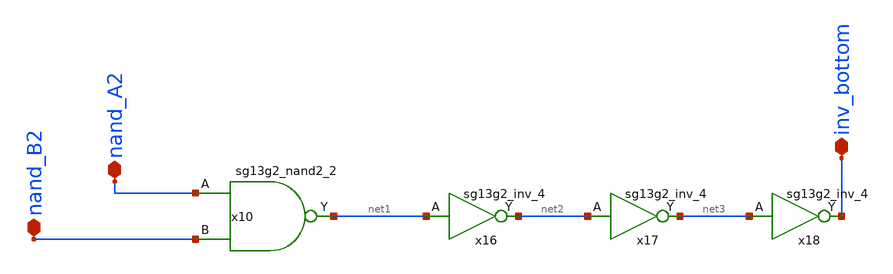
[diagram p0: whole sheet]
** sch_path: 5_Design/4_Layout/Team 5/xschem/clock_5_split4.sch
* IHP-GmbH/IHP-Open-PDK/ihp-sg13g2/libs.tech/xschem/sg13g2_stdcells/sg13g2_inv_4.sch:
* Copyright 2023 IHP PDK Authors
* Licensed under the Apache License, Version 2.0 (the "License");
**.subckt clock_5_split4 inv_bottom nand_A2 nand_B2
*.iopin inv_bottom
*.iopin nand_A2
*.iopin nand_B2
x16 net2 net1 VDD VSS sg13g2_inv_4
x17 net3 net2 VDD VSS sg13g2_inv_4
x18 inv_bottom net3 VDD VSS sg13g2_inv_4
x10 net1 nand_A2 nand_B2 VDD VSS sg13g2_nand2_2
**.ends

* expanding   symbol:  sg13g2_stdcells/sg13g2_inv_4.sym # of pins=2
** sym_path: sg13g2_stdcells/sg13g2_inv_4.sym
** sch_path: sg13g2_stdcells/sg13g2_inv_4.sch
.subckt sg13g2_inv_4 Y A VDD VSS
*.ipin A
*.opin Y
*.iopin VDD
*.iopin VSS
XM1 Y A VSS VSS sg13_lv_nmos w=2.96u l=130.00n ng=4 m=1 mm_ok=1
XM2 Y A VDD VDD sg13_lv_pmos w=4.48u l=130.00n ng=4 m=1 mm_ok=1
.ends


* expanding   symbol:  sg13g2_stdcells/sg13g2_nand2_2.sym # of pins=3
** sym_path: sg13g2_stdcells/sg13g2_nand2_2.sym
** sch_path: sg13g2_stdcells/sg13g2_nand2_2.sch
.subckt sg13g2_nand2_2 Y A B VDD VSS
*.iopin VDD
*.iopin VSS
*.opin Y
*.ipin B
*.ipin A
XM1 Y A net1 VSS sg13_lv_nmos w=1.44u l=130.00n ng=2 m=1 mm_ok=1
XM2 net1 B VSS VSS sg13_lv_nmos w=1.44u l=130.00n ng=2 m=1 mm_ok=1
XM3 Y A VDD VDD sg13_lv_pmos w=2.24u l=130.00n ng=2 m=1 mm_ok=1
XM4 Y B VDD VDD sg13_lv_pmos w=2.24u l=130.00n ng=2 m=1 mm_ok=1
.ends

.end
